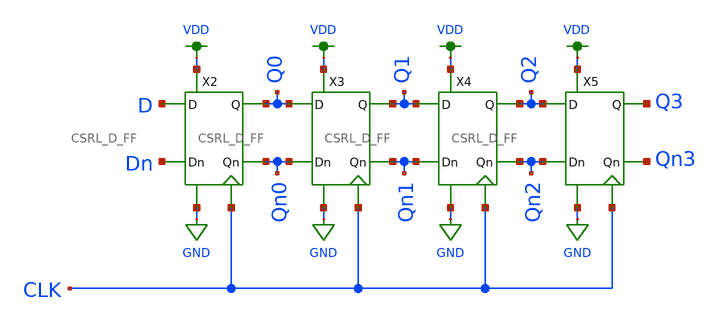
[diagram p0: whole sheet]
** sch_path: schematic/shift_register_lvs.sch
**.subckt shift_register_lvs
X2 Dn D Qn0 Q0 GND VDD CLK CSRL_D_FF
X3 Qn0 Q0 Qn1 Q1 GND VDD CLK CSRL_D_FF
X4 Qn1 Q1 Qn2 Q2 GND VDD CLK CSRL_D_FF
X5 Qn2 Q2 Qn3 Q3 GND VDD CLK CSRL_D_FF
**.ends

* expanding   symbol:  /home/madvlsi/Documents/MADVLSI-MP2/schematic/CSRL_D_FF.sym # of pins=7
** sym_path: /home/madvlsi/Documents/MADVLSI-MP2/schematic/CSRL_D_FF.sym
** sch_path: /home/madvlsi/Documents/MADVLSI-MP2/schematic/CSRL_D_FF.sch
.subckt CSRL_D_FF Dn D Qn Q VN VP CLK
*.ipin Dn
*.ipin D
*.iopin VP
*.iopin VN
*.iopin CLK
*.opin Qn
*.opin Q
XM1 net5 CLK VP VDD sky130_fd_pr__pfet_01v8 L=0.15 W=1 nf=1 ad='int((nf+1)/2) * W/nf * 0.29' as='int((nf+2)/2) * W/nf * 0.29'
+ pd='2*int((nf+1)/2) * (W/nf + 0.29)' ps='2*int((nf+2)/2) * (W/nf + 0.29)' nrd='0.29 / W' nrs='0.29 / W'
+ sa=0 sb=0 sd=0 mult=1 m=1
XM2 net6 CLK VP VDD sky130_fd_pr__pfet_01v8 L=0.15 W=1 nf=1 ad='int((nf+1)/2) * W/nf * 0.29' as='int((nf+2)/2) * W/nf * 0.29'
+ pd='2*int((nf+1)/2) * (W/nf + 0.29)' ps='2*int((nf+2)/2) * (W/nf + 0.29)' nrd='0.29 / W' nrs='0.29 / W'
+ sa=0 sb=0 sd=0 mult=1 m=1
XM3 net3 CLK Q GND sky130_fd_pr__nfet_01v8 L=0.15 W=1 nf=1 ad='int((nf+1)/2) * W/nf * 0.29' as='int((nf+2)/2) * W/nf * 0.29'
+ pd='2*int((nf+1)/2) * (W/nf + 0.29)' ps='2*int((nf+2)/2) * (W/nf + 0.29)' nrd='0.29 / W' nrs='0.29 / W'
+ sa=0 sb=0 sd=0 mult=1 m=1
XM4 net4 CLK Qn GND sky130_fd_pr__nfet_01v8 L=0.15 W=1 nf=1 ad='int((nf+1)/2) * W/nf * 0.29' as='int((nf+2)/2) * W/nf * 0.29'
+ pd='2*int((nf+1)/2) * (W/nf + 0.29)' ps='2*int((nf+2)/2) * (W/nf + 0.29)' nrd='0.29 / W' nrs='0.29 / W'
+ sa=0 sb=0 sd=0 mult=1 m=1
XM5 Q Qn net6 VDD sky130_fd_pr__pfet_01v8 L=0.15 W=1 nf=1 ad='int((nf+1)/2) * W/nf * 0.29' as='int((nf+2)/2) * W/nf * 0.29'
+ pd='2*int((nf+1)/2) * (W/nf + 0.29)' ps='2*int((nf+2)/2) * (W/nf + 0.29)' nrd='0.29 / W' nrs='0.29 / W'
+ sa=0 sb=0 sd=0 mult=1 m=1
XM6 VN Qn Q GND sky130_fd_pr__nfet_01v8 L=0.15 W=1 nf=1 ad='int((nf+1)/2) * W/nf * 0.29' as='int((nf+2)/2) * W/nf * 0.29'
+ pd='2*int((nf+1)/2) * (W/nf + 0.29)' ps='2*int((nf+2)/2) * (W/nf + 0.29)' nrd='0.29 / W' nrs='0.29 / W'
+ sa=0 sb=0 sd=0 mult=1 m=1
XM7 Qn Q net5 VDD sky130_fd_pr__pfet_01v8 L=0.15 W=1 nf=1 ad='int((nf+1)/2) * W/nf * 0.29' as='int((nf+2)/2) * W/nf * 0.29'
+ pd='2*int((nf+1)/2) * (W/nf + 0.29)' ps='2*int((nf+2)/2) * (W/nf + 0.29)' nrd='0.29 / W' nrs='0.29 / W'
+ sa=0 sb=0 sd=0 mult=1 m=1
XM8 VN Q Qn GND sky130_fd_pr__nfet_01v8 L=0.15 W=1 nf=1 ad='int((nf+1)/2) * W/nf * 0.29' as='int((nf+2)/2) * W/nf * 0.29'
+ pd='2*int((nf+1)/2) * (W/nf + 0.29)' ps='2*int((nf+2)/2) * (W/nf + 0.29)' nrd='0.29 / W' nrs='0.29 / W'
+ sa=0 sb=0 sd=0 mult=1 m=1
XM9 net4 CLK Dn VDD sky130_fd_pr__pfet_01v8 L=0.15 W=1 nf=1 ad='int((nf+1)/2) * W/nf * 0.29' as='int((nf+2)/2) * W/nf * 0.29'
+ pd='2*int((nf+1)/2) * (W/nf + 0.29)' ps='2*int((nf+2)/2) * (W/nf + 0.29)' nrd='0.29 / W' nrs='0.29 / W'
+ sa=0 sb=0 sd=0 mult=1 m=1
XM10 net3 CLK D VDD sky130_fd_pr__pfet_01v8 L=0.15 W=1 nf=1 ad='int((nf+1)/2) * W/nf * 0.29' as='int((nf+2)/2) * W/nf * 0.29'
+ pd='2*int((nf+1)/2) * (W/nf + 0.29)' ps='2*int((nf+2)/2) * (W/nf + 0.29)' nrd='0.29 / W' nrs='0.29 / W'
+ sa=0 sb=0 sd=0 mult=1 m=1
XM11 VN CLK net1 GND sky130_fd_pr__nfet_01v8 L=0.15 W=2 nf=1 ad='int((nf+1)/2) * W/nf * 0.29' as='int((nf+2)/2) * W/nf * 0.29'
+ pd='2*int((nf+1)/2) * (W/nf + 0.29)' ps='2*int((nf+2)/2) * (W/nf + 0.29)' nrd='0.29 / W' nrs='0.29 / W'
+ sa=0 sb=0 sd=0 mult=1 m=1
XM12 VN CLK net2 GND sky130_fd_pr__nfet_01v8 L=0.15 W=1 nf=1 ad='int((nf+1)/2) * W/nf * 0.29' as='int((nf+2)/2) * W/nf * 0.29'
+ pd='2*int((nf+1)/2) * (W/nf + 0.29)' ps='2*int((nf+2)/2) * (W/nf + 0.29)' nrd='0.29 / W' nrs='0.29 / W'
+ sa=0 sb=0 sd=0 mult=1 m=1
XM13 VP net3 net4 VDD sky130_fd_pr__pfet_01v8 L=0.15 W=1 nf=1 ad='int((nf+1)/2) * W/nf * 0.29' as='int((nf+2)/2) * W/nf * 0.29'
+ pd='2*int((nf+1)/2) * (W/nf + 0.29)' ps='2*int((nf+2)/2) * (W/nf + 0.29)' nrd='0.29 / W' nrs='0.29 / W'
+ sa=0 sb=0 sd=0 mult=1 m=1
XM14 VP net4 net3 VDD sky130_fd_pr__pfet_01v8 L=0.15 W=1 nf=1 ad='int((nf+1)/2) * W/nf * 0.29' as='int((nf+2)/2) * W/nf * 0.29'
+ pd='2*int((nf+1)/2) * (W/nf + 0.29)' ps='2*int((nf+2)/2) * (W/nf + 0.29)' nrd='0.29 / W' nrs='0.29 / W'
+ sa=0 sb=0 sd=0 mult=1 m=1
XM15 net3 net4 net1 GND sky130_fd_pr__nfet_01v8 L=0.15 W=1 nf=1 ad='int((nf+1)/2) * W/nf * 0.29' as='int((nf+2)/2) * W/nf * 0.29'
+ pd='2*int((nf+1)/2) * (W/nf + 0.29)' ps='2*int((nf+2)/2) * (W/nf + 0.29)' nrd='0.29 / W' nrs='0.29 / W'
+ sa=0 sb=0 sd=0 mult=1 m=1
XM16 net4 net3 net2 GND sky130_fd_pr__nfet_01v8 L=0.15 W=1 nf=1 ad='int((nf+1)/2) * W/nf * 0.29' as='int((nf+2)/2) * W/nf * 0.29'
+ pd='2*int((nf+1)/2) * (W/nf + 0.29)' ps='2*int((nf+2)/2) * (W/nf + 0.29)' nrd='0.29 / W' nrs='0.29 / W'
+ sa=0 sb=0 sd=0 mult=1 m=1
XM17 VN CLK net2 GND sky130_fd_pr__nfet_01v8 L=0.15 W=1 nf=1 ad='int((nf+1)/2) * W/nf * 0.29' as='int((nf+2)/2) * W/nf * 0.29'
+ pd='2*int((nf+1)/2) * (W/nf + 0.29)' ps='2*int((nf+2)/2) * (W/nf + 0.29)' nrd='0.29 / W' nrs='0.29 / W'
+ sa=0 sb=0 sd=0 mult=1 m=1
XM18 VN CLK net1 GND sky130_fd_pr__nfet_01v8 L=0.15 W=2 nf=1 ad='int((nf+1)/2) * W/nf * 0.29' as='int((nf+2)/2) * W/nf * 0.29'
+ pd='2*int((nf+1)/2) * (W/nf + 0.29)' ps='2*int((nf+2)/2) * (W/nf + 0.29)' nrd='0.29 / W' nrs='0.29 / W'
+ sa=0 sb=0 sd=0 mult=1 m=1
.ends

.GLOBAL GND
.GLOBAL VDD
.end
